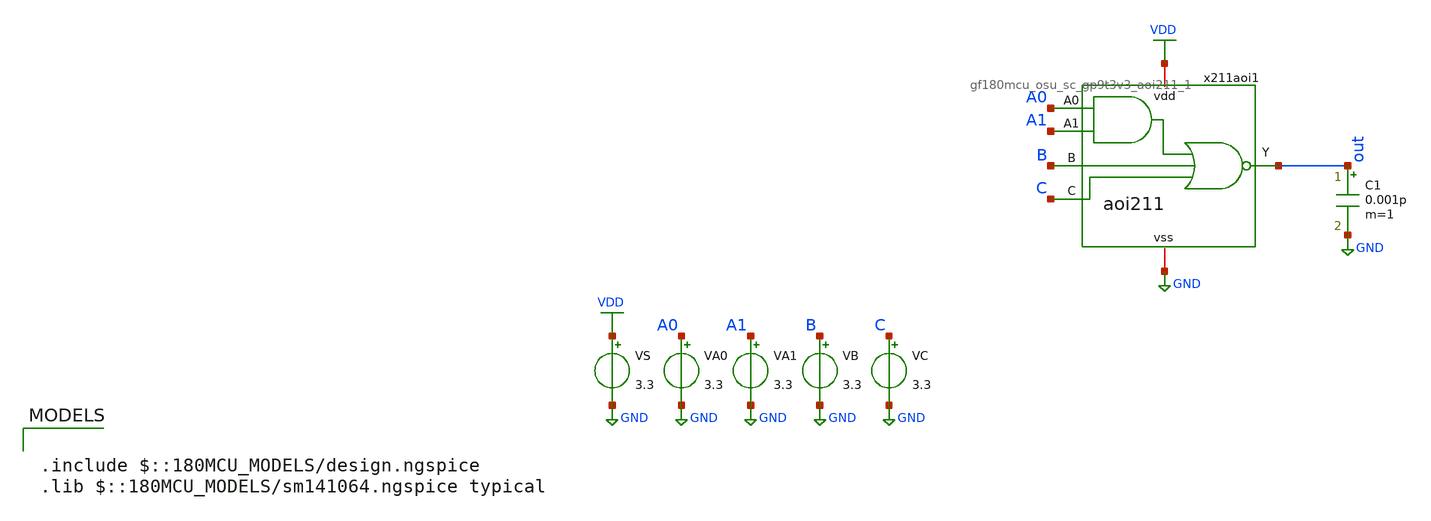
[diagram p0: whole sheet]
** sch_path: designs/aoi211/gf180mcu_osu_sc_9p9t3v3_aoi211_1_tb_2.sch
**.subckt gf180mcu_osu_sc_9p9t3v3_aoi211_1_tb_2
VA0 A0 GND 3.3
VA1 A1 GND 3.3
VB B GND 3.3
VC C GND 3.3
VS VDD GND 3.3
x211aoi1 VDD A1 A0 B C out GND gf180mcu_osu_sc_gp9t3v3_aoi211_1
C1 out GND 0.001p m=1
**** begin user architecture code


.control
save all
** Define input signal
let fsig = 1Meg
let tperA0 = 1/fsig
let tperA1 = 2*tperA0
let tperB = 4*tperA0
let tperC = 8*tperA0
let tfr = 0.01*tperA0
let tonA0 = 0.5*tperA0-tfr
let tonA1 = 0.5*tperA1-tfr
let tonB = 0.5*tperB-tfr
let tonC = 0.5*tperC-tfr

** Define transient params
let tstop = 8*tperA0
let tstep = 0.001*tperA0

** Set Sources
** alter @VA0[DC] = 0.0
** alter @VA1[DC] = 0.0
** alter @VB[DC] = 0.0
** alter @VC[DC] = 0.0
alter @VA0[PULSE] = [ 3.3 0 0 $&tfr $&tfr $&tonA0 $&tperA0 0 ]
alter @VA1[PULSE] = [ 3.3 0 0 $&tfr $&tfr $&tonA1 $&tperA1 0 ]
alter @VB[PULSE] = [ 3.3 0 0 $&tfr $&tfr $&tonB $&tperB 0 ]
alter @VC[PULSE] = [ 3.3 0 0 $&tfr $&tfr $&tonC $&tperC 0 ]

** Simulations op
** dc VA0 0 3.3 0.01
** dc VA1 0 3.3 0.01
** dc VB 0 3.3 0.01
** dc VC 0 3.3 0.01
tran $&tstep $&tstop

let start_point = 0.001*tstop

* Measure TPLH: input rising triggers output rising
  meas tran TPLH TRIG v(a1) VAL=0.5*3.3 FALL=1
  + TARG v(out) VAL=0.5*3.3 RISE=1
  + from=10.2u

  * Measure TPHL: input falling triggers output falling
  meas tran TPHL TRIG v(a1) VAL=0.5*3.3 RISE=1
  + TARG v(out) VAL=0.5*3.3 FALL=1
  + from=11.8u

  * Measure Rise Time: output from 10% to 90%
  meas tran Trise TRIG v(out) VAL=0.1*3.3 RISE=LAST
  + TARG v(out) VAL=0.9*3.3 RISE=lAST
  + from=$&start_point

  * Measure Fall Time: output from 90% to 10%
  meas tran Tfall TRIG v(out) VAL=0.9*3.3 FALL=1
  + TARG v(out) VAL=0.1*3.3 FALL=2
  + from=$&start_point

meas tran Vpeak MAX v(out)  from=$&start_point

write /foss/designs/SSCS-Chipaton-2025_ChipiChapa/designs/aoi211/gf180mcu_gp9t3v3__aoi211_1_tb_2.raw
.endc



.include $::180MCU_MODELS/design.ngspice
.lib $::180MCU_MODELS/sm141064.ngspice typical

**** end user architecture code
**.ends
.GLOBAL GND
.GLOBAL VDD
.end
